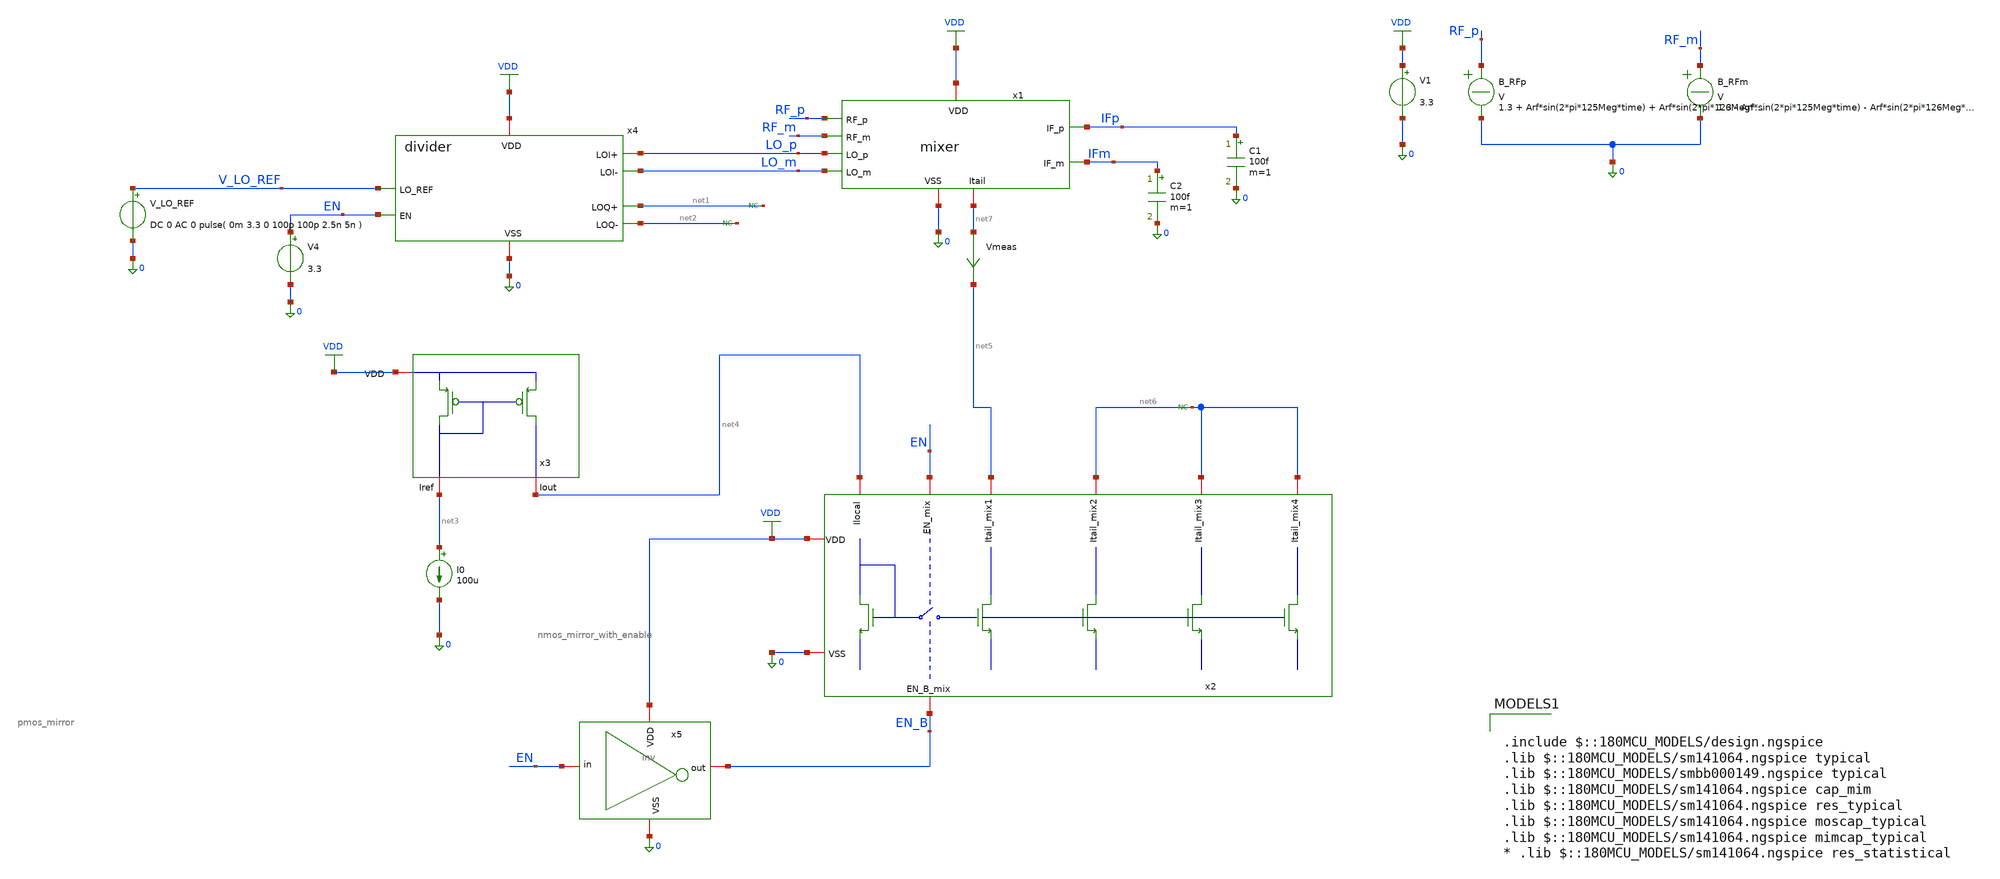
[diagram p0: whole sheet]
** sch_path: designs/mixer/testbench/mixer_iip3_tb.sch
**.subckt mixer_iip3_tb
V1 VDD 0 3.3
C1 IFp 0 100f m=1
C2 IFm 0 100f m=1
x1 IFp RF_p VDD 0 IFm RF_m LO_p net7 LO_m mixer
B_RFp RF_p 0 V = 1.3 + Arf*sin(2*pi*125Meg*time) + Arf*sin(2*pi*126Meg*time)
B_RFm RF_m 0 V = 1.3 - Arf*sin(2*pi*125Meg*time) - Arf*sin(2*pi*126Meg*time)
V_LO_REF V_LO_REF 0 DC 0 AC 0 pulse( 0m 3.3 0 100p 100p 2.5n 5n )
x4 VDD 0 V_LO_REF LO_p LO_m net1 net2 EN divider
* noconn #net1
* noconn #net2
V4 EN 0 3.3
x3 VDD net4 net3 pmos_mirror
I0 net3 0 100u
x2 net6 net6 net4 VDD EN net5 0 EN_B net6 nmos_mirror_with_enable
* noconn #net6
x5 VDD EN_B EN 0 inv
Vmeas net7 net5 0
.save i(vmeas)
**** begin user architecture code


.param Arf=10m
.control

destroy all

op
echo Itail
print i(vmeas)

foreach A 30m
	alterparam Arf = $A
	reset
	save v(ifp) v(ifm)
	tran 0.1n 25u ;transient sim

	let vif = V(IFp)-V(IFm)

	fft vif
	plot db(mag(vif)) vs frequency xlimit 20Meg 30Meg
	plot mag(vif) vs frequency xlimit 20Meg 30Meg
end

.endc



.include $::180MCU_MODELS/design.ngspice
.lib $::180MCU_MODELS/sm141064.ngspice typical
.lib $::180MCU_MODELS/smbb000149.ngspice typical
.lib $::180MCU_MODELS/sm141064.ngspice cap_mim
.lib $::180MCU_MODELS/sm141064.ngspice res_typical
.lib $::180MCU_MODELS/sm141064.ngspice moscap_typical
.lib $::180MCU_MODELS/sm141064.ngspice mimcap_typical
* .lib $::180MCU_MODELS/sm141064.ngspice res_statistical

**** end user architecture code
**.ends
.GLOBAL VDD
.end
